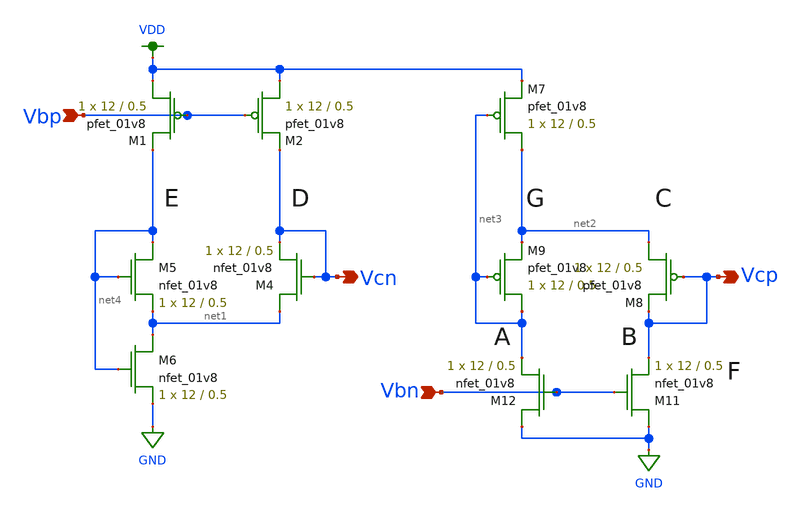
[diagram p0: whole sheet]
** sch_path: xschem/VGen.sch
**.subckt VGen Vcp Vbp Vbn Vcn
*.opin Vcp
*.ipin Vbp
*.ipin Vbn
*.opin Vcn
XM5 net4 net4 net1 GND sky130_fd_pr__nfet_01v8 L=0.5 W=12 nf=1 ad='int((nf+1)/2) * W/nf * 0.29' as='int((nf+2)/2) * W/nf * 0.29'
+ pd='2*int((nf+1)/2) * (W/nf + 0.29)' ps='2*int((nf+2)/2) * (W/nf + 0.29)' nrd='0.29 / W' nrs='0.29 / W'
+ sa=0 sb=0 sd=0 mult=1 m=1
XM6 net1 net4 GND GND sky130_fd_pr__nfet_01v8 L=0.5 W=12 nf=1 ad='int((nf+1)/2) * W/nf * 0.29' as='int((nf+2)/2) * W/nf * 0.29'
+ pd='2*int((nf+1)/2) * (W/nf + 0.29)' ps='2*int((nf+2)/2) * (W/nf + 0.29)' nrd='0.29 / W' nrs='0.29 / W'
+ sa=0 sb=0 sd=0 mult=1 m=1
XM4 net1 Vcn Vcn GND sky130_fd_pr__nfet_01v8 L=0.5 W=12 nf=1 ad='int((nf+1)/2) * W/nf * 0.29' as='int((nf+2)/2) * W/nf * 0.29'
+ pd='2*int((nf+1)/2) * (W/nf + 0.29)' ps='2*int((nf+2)/2) * (W/nf + 0.29)' nrd='0.29 / W' nrs='0.29 / W'
+ sa=0 sb=0 sd=0 mult=1 m=1
XM1 VDD Vbp net4 VDD sky130_fd_pr__pfet_01v8 L=0.5 W=12 nf=1 ad='int((nf+1)/2) * W/nf * 0.29' as='int((nf+2)/2) * W/nf * 0.29'
+ pd='2*int((nf+1)/2) * (W/nf + 0.29)' ps='2*int((nf+2)/2) * (W/nf + 0.29)' nrd='0.29 / W' nrs='0.29 / W'
+ sa=0 sb=0 sd=0 mult=1 m=1
XM2 VDD Vbp Vcn VDD sky130_fd_pr__pfet_01v8 L=0.5 W=12 nf=1 ad='int((nf+1)/2) * W/nf * 0.29' as='int((nf+2)/2) * W/nf * 0.29'
+ pd='2*int((nf+1)/2) * (W/nf + 0.29)' ps='2*int((nf+2)/2) * (W/nf + 0.29)' nrd='0.29 / W' nrs='0.29 / W'
+ sa=0 sb=0 sd=0 mult=1 m=1
XM9 net3 net3 net2 VDD sky130_fd_pr__pfet_01v8 L=0.5 W=12 nf=1 ad='int((nf+1)/2) * W/nf * 0.29' as='int((nf+2)/2) * W/nf * 0.29'
+ pd='2*int((nf+1)/2) * (W/nf + 0.29)' ps='2*int((nf+2)/2) * (W/nf + 0.29)' nrd='0.29 / W' nrs='0.29 / W'
+ sa=0 sb=0 sd=0 mult=1 m=1
XM11 GND Vbn Vcp GND sky130_fd_pr__nfet_01v8 L=0.5 W=12 nf=1 ad='int((nf+1)/2) * W/nf * 0.29' as='int((nf+2)/2) * W/nf * 0.29'
+ pd='2*int((nf+1)/2) * (W/nf + 0.29)' ps='2*int((nf+2)/2) * (W/nf + 0.29)' nrd='0.29 / W' nrs='0.29 / W'
+ sa=0 sb=0 sd=0 mult=1 m=1
XM8 net2 Vcp Vcp VDD sky130_fd_pr__pfet_01v8 L=0.5 W=12 nf=1 ad='int((nf+1)/2) * W/nf * 0.29' as='int((nf+2)/2) * W/nf * 0.29'
+ pd='2*int((nf+1)/2) * (W/nf + 0.29)' ps='2*int((nf+2)/2) * (W/nf + 0.29)' nrd='0.29 / W' nrs='0.29 / W'
+ sa=0 sb=0 sd=0 mult=1 m=1
XM12 GND Vbn net3 GND sky130_fd_pr__nfet_01v8 L=0.5 W=12 nf=1 ad='int((nf+1)/2) * W/nf * 0.29' as='int((nf+2)/2) * W/nf * 0.29'
+ pd='2*int((nf+1)/2) * (W/nf + 0.29)' ps='2*int((nf+2)/2) * (W/nf + 0.29)' nrd='0.29 / W' nrs='0.29 / W'
+ sa=0 sb=0 sd=0 mult=1 m=1
XM7 net2 net3 VDD VDD sky130_fd_pr__pfet_01v8 L=0.5 W=12 nf=1 ad='int((nf+1)/2) * W/nf * 0.29' as='int((nf+2)/2) * W/nf * 0.29'
+ pd='2*int((nf+1)/2) * (W/nf + 0.29)' ps='2*int((nf+2)/2) * (W/nf + 0.29)' nrd='0.29 / W' nrs='0.29 / W'
+ sa=0 sb=0 sd=0 mult=1 m=1
**.ends
.GLOBAL GND
.GLOBAL VDD
.end
